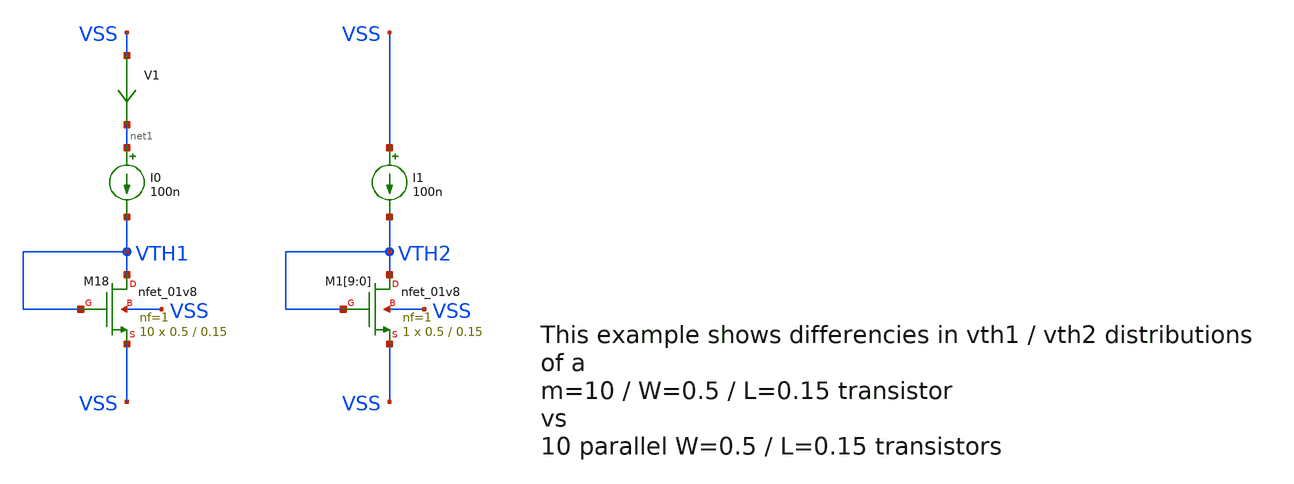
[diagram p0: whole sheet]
** sch_path: sky130A/xschem_libs/sky130_tests_ase/sky130_mismatch/schematic/sky130_mismatch.sch
**.subckt sky130_mismatch
XM18 VTH1 VTH1 VSS VSS sky130_fd_pr__nfet_01v8 L=0.15 W=0.5 nf=1 ad='int((1 + 1)/2) * 0.5 / 1 * 0.29'
+ as='int((1 + 2)/2) * 0.5 / 1 * 0.29' pd='2*int((1 + 1)/2) * (0.5 / 1 + 0.29)' ps='2*int((1 + 2)/2) * (0.5 / 1 + 0.29)'
+ nrd='0.29 / 0.5 ' nrs='0.29 / 0.5 ' sa=0 sb=0 sd=0 mult=10 m=10
I0 net1 VTH1 100n
XM1[9] VTH2 VTH2 VSS VSS sky130_fd_pr__nfet_01v8 L=0.15 W=0.5 nf=1 ad='int((1 + 1)/2) * 0.5 / 1 * 0.29'
+ as='int((1 + 2)/2) * 0.5 / 1 * 0.29' pd='2*int((1 + 1)/2) * (0.5 / 1 + 0.29)' ps='2*int((1 + 2)/2) * (0.5 / 1 + 0.29)'
+ nrd='0.29 / 0.5 ' nrs='0.29 / 0.5 ' sa=0 sb=0 sd=0 mult=1 m=1
XM1[8] VTH2 VTH2 VSS VSS sky130_fd_pr__nfet_01v8 L=0.15 W=0.5 nf=1 ad='int((1 + 1)/2) * 0.5 / 1 * 0.29'
+ as='int((1 + 2)/2) * 0.5 / 1 * 0.29' pd='2*int((1 + 1)/2) * (0.5 / 1 + 0.29)' ps='2*int((1 + 2)/2) * (0.5 / 1 + 0.29)'
+ nrd='0.29 / 0.5 ' nrs='0.29 / 0.5 ' sa=0 sb=0 sd=0 mult=1 m=1
XM1[7] VTH2 VTH2 VSS VSS sky130_fd_pr__nfet_01v8 L=0.15 W=0.5 nf=1 ad='int((1 + 1)/2) * 0.5 / 1 * 0.29'
+ as='int((1 + 2)/2) * 0.5 / 1 * 0.29' pd='2*int((1 + 1)/2) * (0.5 / 1 + 0.29)' ps='2*int((1 + 2)/2) * (0.5 / 1 + 0.29)'
+ nrd='0.29 / 0.5 ' nrs='0.29 / 0.5 ' sa=0 sb=0 sd=0 mult=1 m=1
XM1[6] VTH2 VTH2 VSS VSS sky130_fd_pr__nfet_01v8 L=0.15 W=0.5 nf=1 ad='int((1 + 1)/2) * 0.5 / 1 * 0.29'
+ as='int((1 + 2)/2) * 0.5 / 1 * 0.29' pd='2*int((1 + 1)/2) * (0.5 / 1 + 0.29)' ps='2*int((1 + 2)/2) * (0.5 / 1 + 0.29)'
+ nrd='0.29 / 0.5 ' nrs='0.29 / 0.5 ' sa=0 sb=0 sd=0 mult=1 m=1
XM1[5] VTH2 VTH2 VSS VSS sky130_fd_pr__nfet_01v8 L=0.15 W=0.5 nf=1 ad='int((1 + 1)/2) * 0.5 / 1 * 0.29'
+ as='int((1 + 2)/2) * 0.5 / 1 * 0.29' pd='2*int((1 + 1)/2) * (0.5 / 1 + 0.29)' ps='2*int((1 + 2)/2) * (0.5 / 1 + 0.29)'
+ nrd='0.29 / 0.5 ' nrs='0.29 / 0.5 ' sa=0 sb=0 sd=0 mult=1 m=1
XM1[4] VTH2 VTH2 VSS VSS sky130_fd_pr__nfet_01v8 L=0.15 W=0.5 nf=1 ad='int((1 + 1)/2) * 0.5 / 1 * 0.29'
+ as='int((1 + 2)/2) * 0.5 / 1 * 0.29' pd='2*int((1 + 1)/2) * (0.5 / 1 + 0.29)' ps='2*int((1 + 2)/2) * (0.5 / 1 + 0.29)'
+ nrd='0.29 / 0.5 ' nrs='0.29 / 0.5 ' sa=0 sb=0 sd=0 mult=1 m=1
XM1[3] VTH2 VTH2 VSS VSS sky130_fd_pr__nfet_01v8 L=0.15 W=0.5 nf=1 ad='int((1 + 1)/2) * 0.5 / 1 * 0.29'
+ as='int((1 + 2)/2) * 0.5 / 1 * 0.29' pd='2*int((1 + 1)/2) * (0.5 / 1 + 0.29)' ps='2*int((1 + 2)/2) * (0.5 / 1 + 0.29)'
+ nrd='0.29 / 0.5 ' nrs='0.29 / 0.5 ' sa=0 sb=0 sd=0 mult=1 m=1
XM1[2] VTH2 VTH2 VSS VSS sky130_fd_pr__nfet_01v8 L=0.15 W=0.5 nf=1 ad='int((1 + 1)/2) * 0.5 / 1 * 0.29'
+ as='int((1 + 2)/2) * 0.5 / 1 * 0.29' pd='2*int((1 + 1)/2) * (0.5 / 1 + 0.29)' ps='2*int((1 + 2)/2) * (0.5 / 1 + 0.29)'
+ nrd='0.29 / 0.5 ' nrs='0.29 / 0.5 ' sa=0 sb=0 sd=0 mult=1 m=1
XM1[1] VTH2 VTH2 VSS VSS sky130_fd_pr__nfet_01v8 L=0.15 W=0.5 nf=1 ad='int((1 + 1)/2) * 0.5 / 1 * 0.29'
+ as='int((1 + 2)/2) * 0.5 / 1 * 0.29' pd='2*int((1 + 1)/2) * (0.5 / 1 + 0.29)' ps='2*int((1 + 2)/2) * (0.5 / 1 + 0.29)'
+ nrd='0.29 / 0.5 ' nrs='0.29 / 0.5 ' sa=0 sb=0 sd=0 mult=1 m=1
XM1[0] VTH2 VTH2 VSS VSS sky130_fd_pr__nfet_01v8 L=0.15 W=0.5 nf=1 ad='int((1 + 1)/2) * 0.5 / 1 * 0.29'
+ as='int((1 + 2)/2) * 0.5 / 1 * 0.29' pd='2*int((1 + 1)/2) * (0.5 / 1 + 0.29)' ps='2*int((1 + 2)/2) * (0.5 / 1 + 0.29)'
+ nrd='0.29 / 0.5 ' nrs='0.29 / 0.5 ' sa=0 sb=0 sd=0 mult=1 m=1
V1 VSS net1 0
.save i(v1)
I1 VSS VTH2 100n
**.ends
.end
